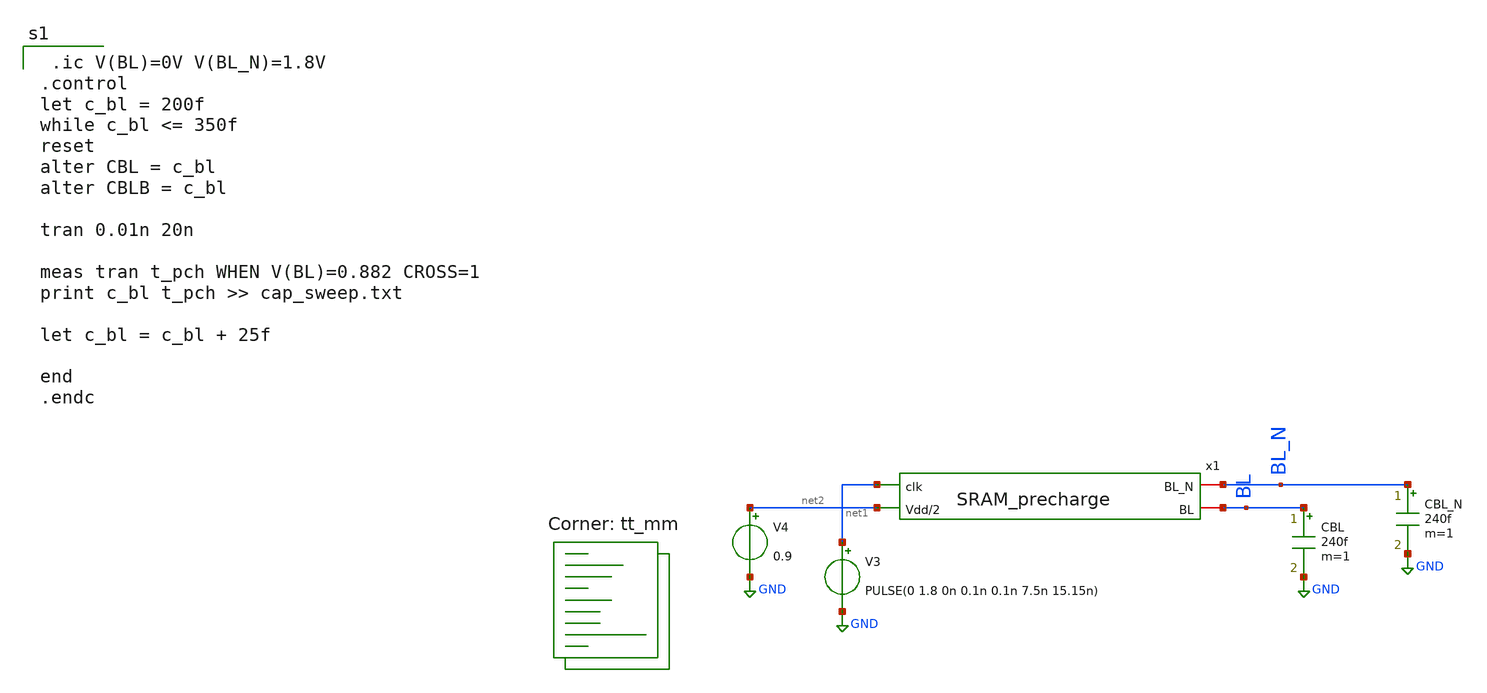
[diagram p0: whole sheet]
** sch_path: analog/schematics/tb.sch
**.subckt tb
CBL_N BL_N GND 240f m=1
CBL BL GND 240f m=1
V3 net1 GND PULSE(0 1.8 0n 0.1n 0.1n 7.5n 15.15n)
V4 net2 GND 0.9
x1 BL_N BL net1 net2 SRAM_precharge
**** begin user architecture code

 .ic V(BL)=0V V(BL_N)=1.8V
.control
let c_bl = 200f
while c_bl <= 350f
reset
alter CBL = c_bl
alter CBLB = c_bl

tran 0.01n 20n

meas tran t_pch WHEN V(BL)=0.882 CROSS=1
print c_bl t_pch >> cap_sweep.txt

let c_bl = c_bl + 25f

end
.endc

.lib $::SKYWATER_MODELS/sky130.lib.spice tt_mm
**** end user architecture code
**.ends
.GLOBAL GND
.end
